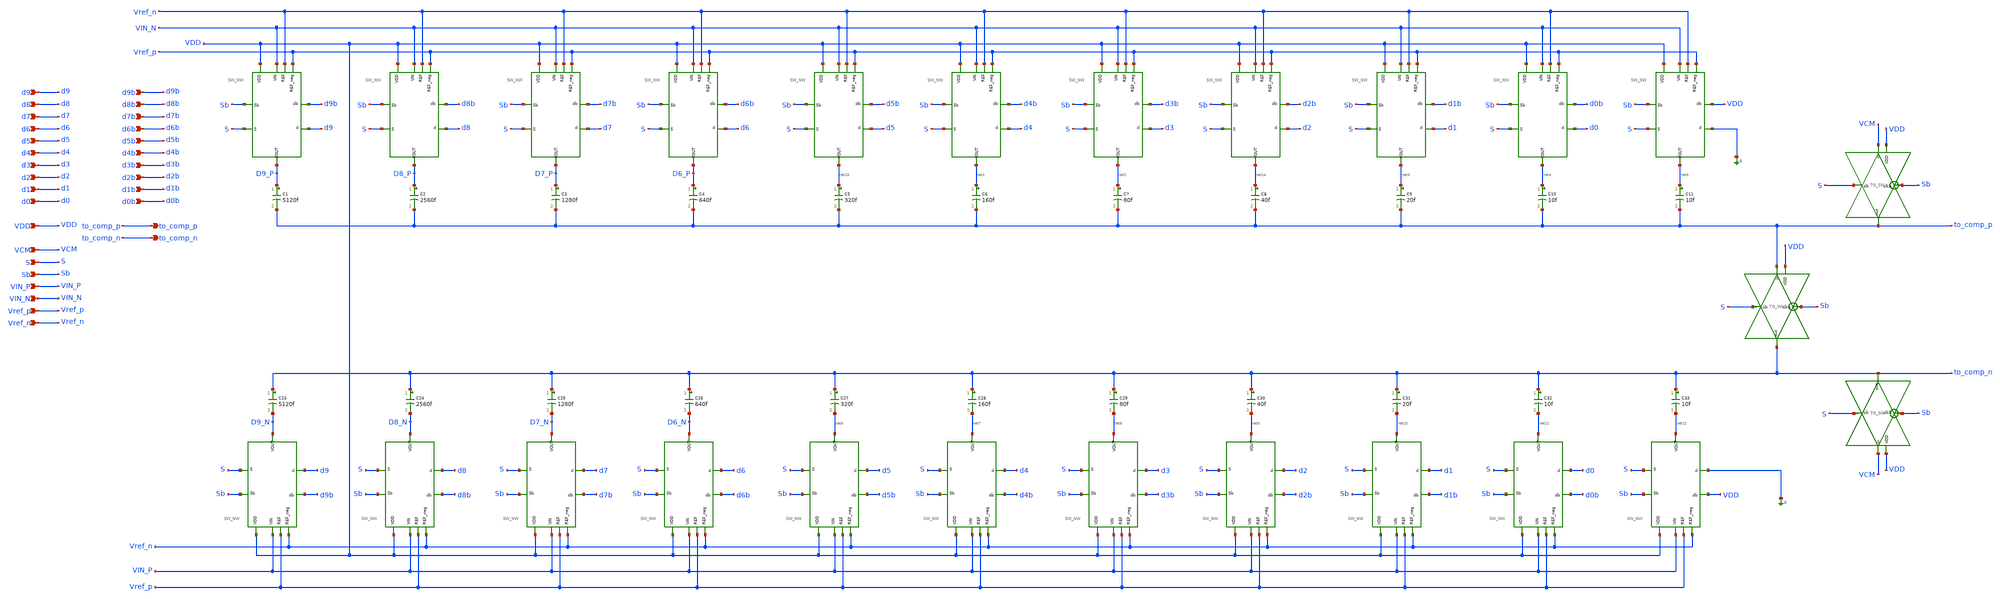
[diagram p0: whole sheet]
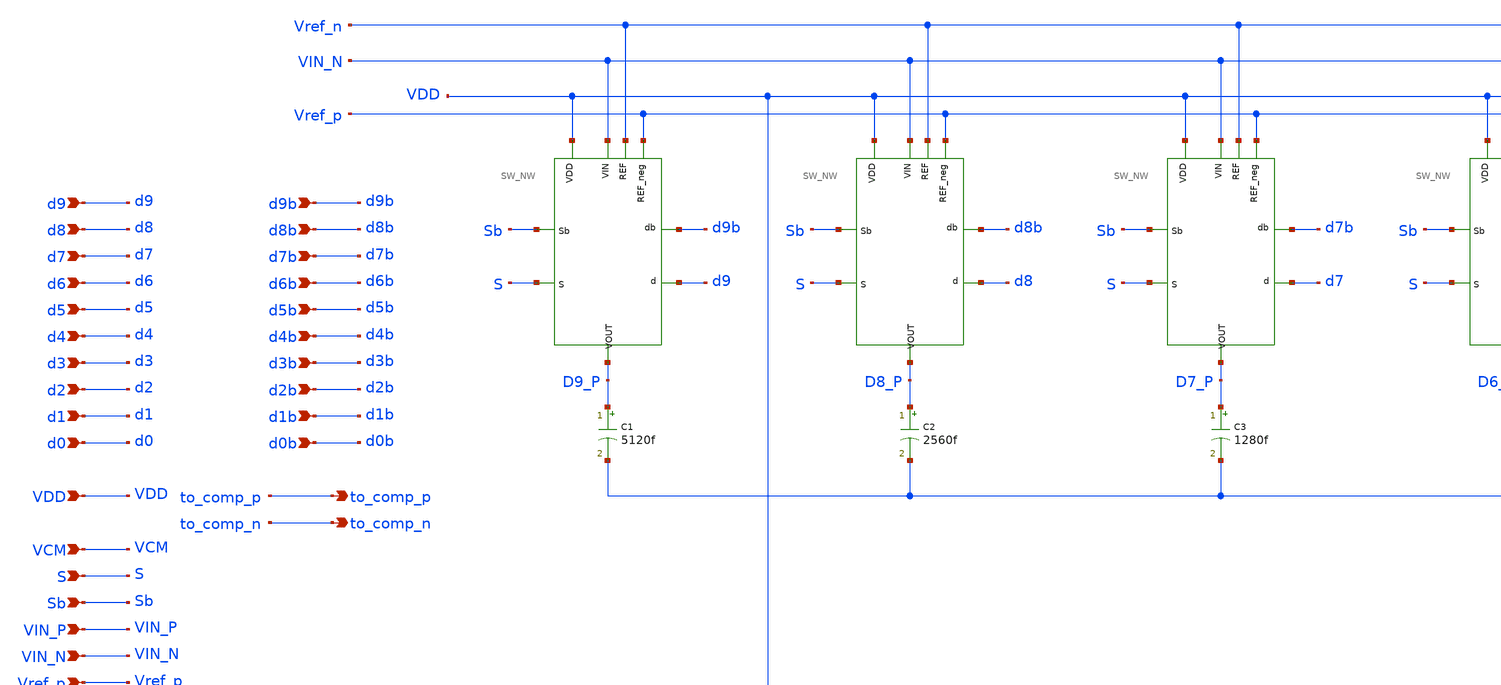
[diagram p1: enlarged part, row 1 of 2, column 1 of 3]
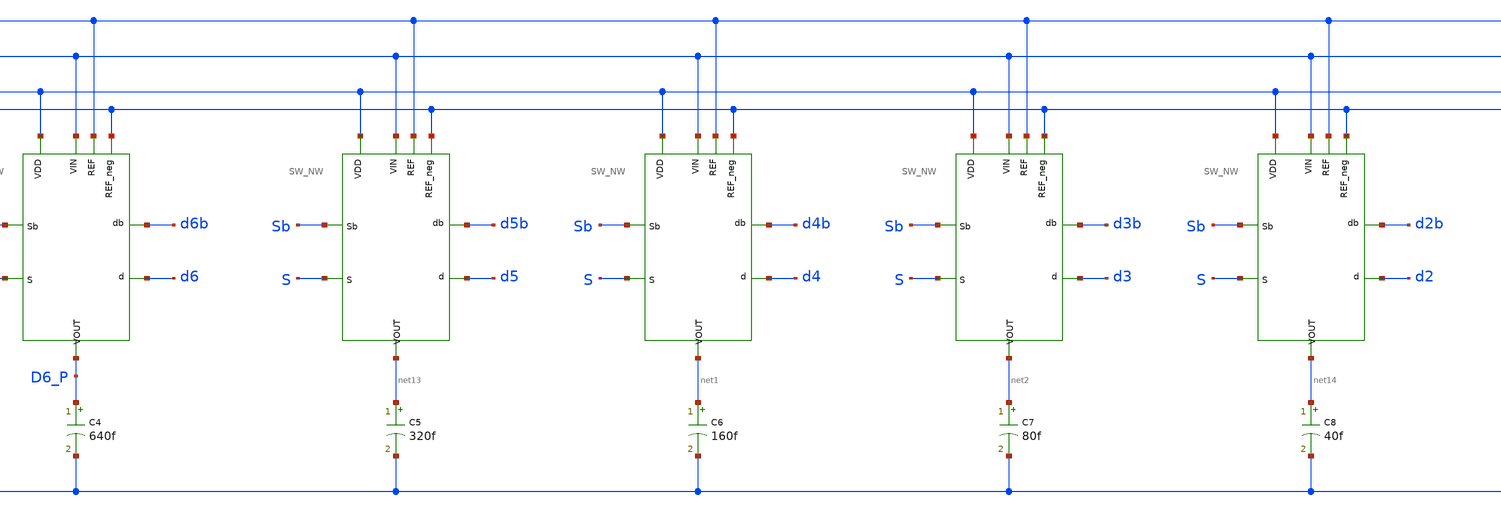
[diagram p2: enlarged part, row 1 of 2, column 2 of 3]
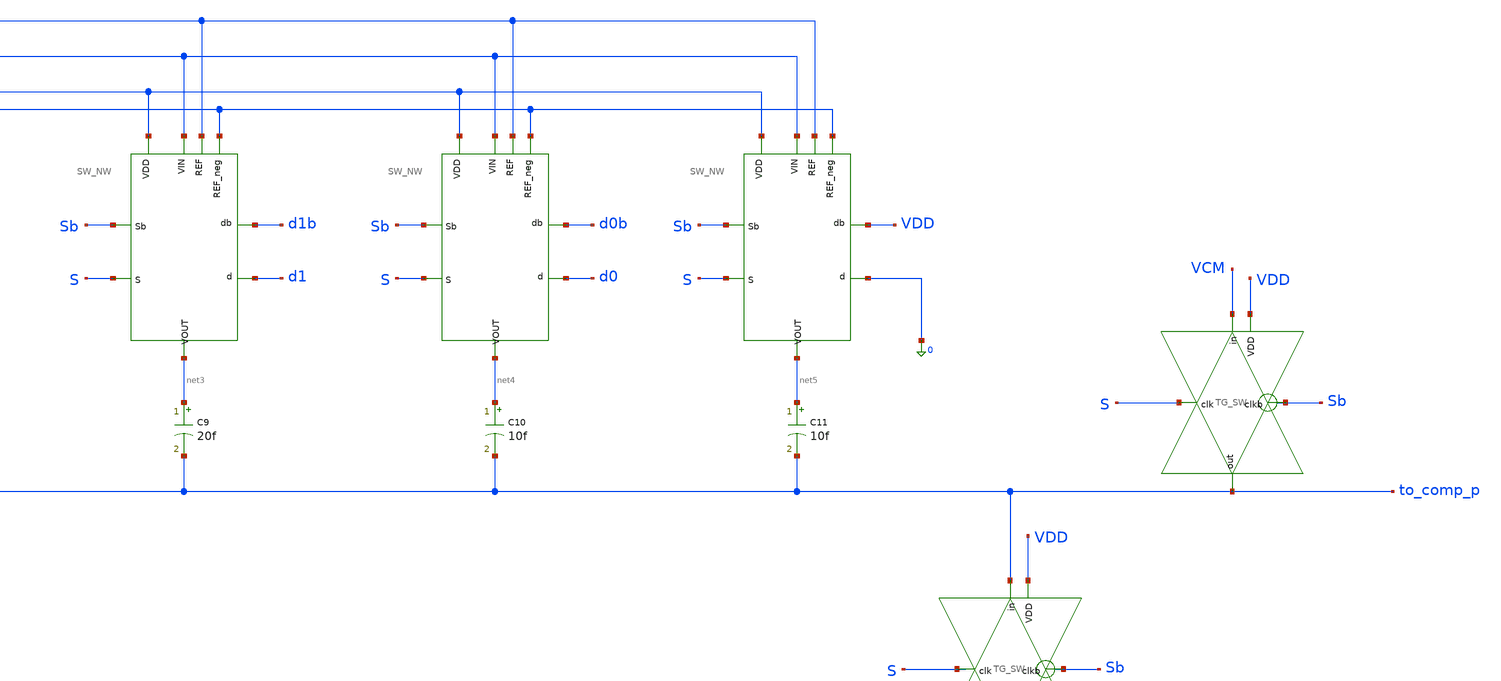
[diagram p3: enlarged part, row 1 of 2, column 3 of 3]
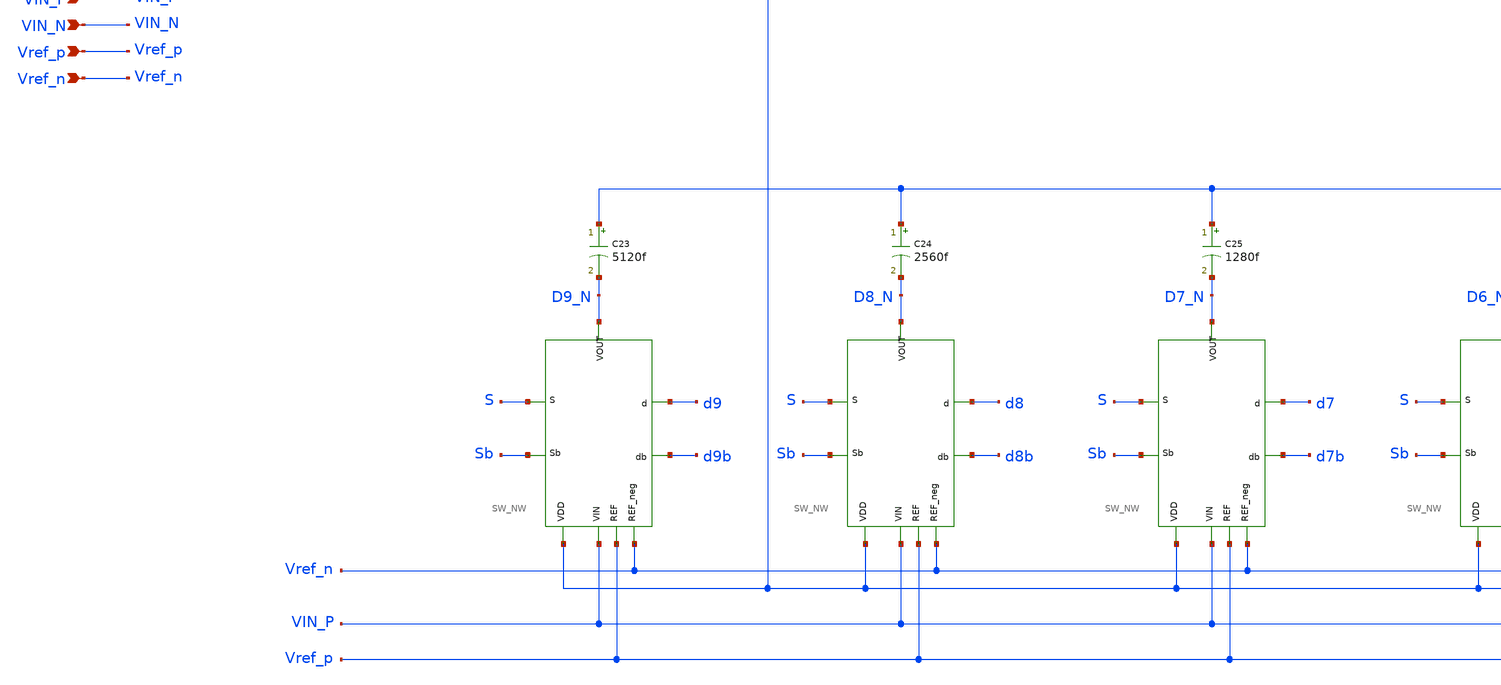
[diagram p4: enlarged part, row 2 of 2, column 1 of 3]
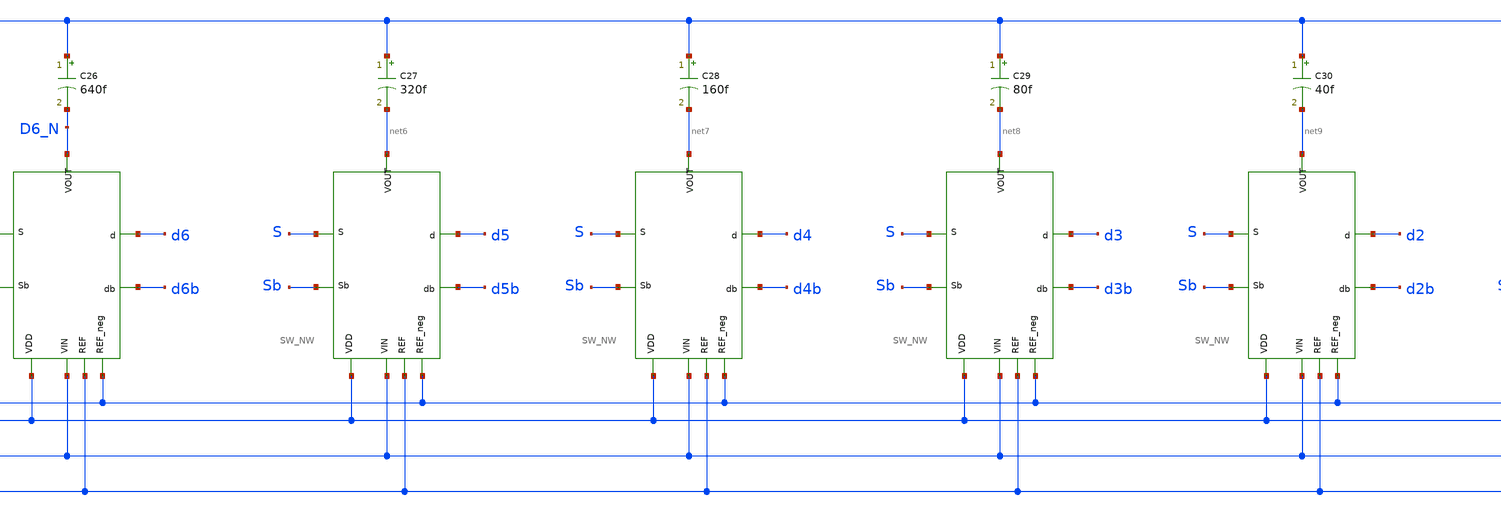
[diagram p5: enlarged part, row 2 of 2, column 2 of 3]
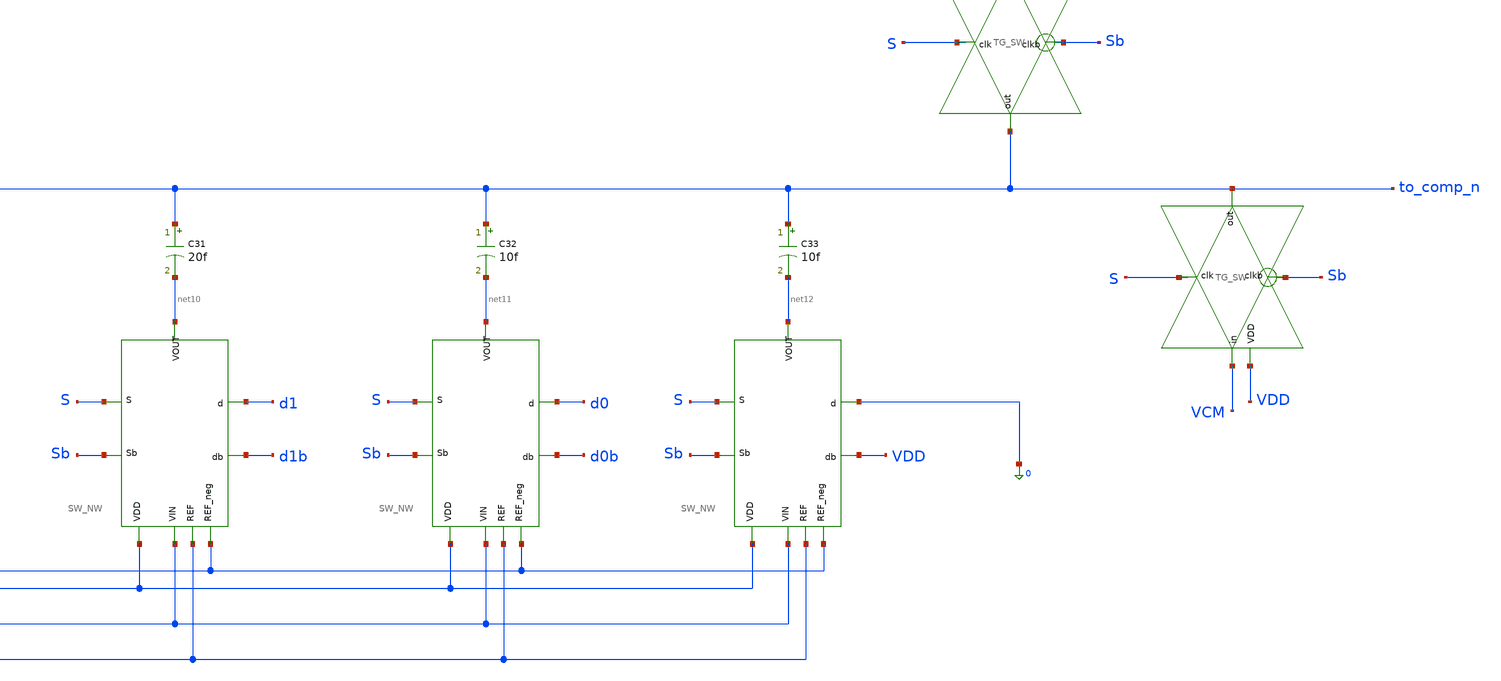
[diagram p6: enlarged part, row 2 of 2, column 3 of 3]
** sch_path: Design_Files/IC Design/Schematic/SAR_ADC_BLOCKS/CDAC/CDAC.sch
**.subckt CDAC d7 d7b d6 d6b d9 d9b d8 d8b d3 d3b d2 d2b d5 d5b d4 d4b d1 d1b d0 d0b VCM S VDD VIN_N
*+ Vref_p Sb VIN_P Vref_n to_comp_p to_comp_n
*.ipin d7
*.ipin d7b
*.ipin d6
*.ipin d6b
*.ipin d9
*.ipin d9b
*.ipin d8
*.ipin d8b
*.ipin d3
*.ipin d3b
*.ipin d2
*.ipin d2b
*.ipin d5
*.ipin d5b
*.ipin d4
*.ipin d4b
*.ipin d1
*.ipin d1b
*.ipin d0
*.ipin d0b
*.ipin VCM
*.ipin S
*.ipin VDD
*.ipin VIN_N
*.ipin Vref_p
*.ipin Sb
*.ipin VIN_P
*.ipin Vref_n
*.opin to_comp_p
*.opin to_comp_n
C1 D9_P to_comp_p 5120f m=1
C2 D8_P to_comp_p 2560f m=1
C3 D7_P to_comp_p 1280f m=1
C4 D6_P to_comp_p 640f m=1
C5 net13 to_comp_p 320f m=1
C6 net1 to_comp_p 160f m=1
C7 net2 to_comp_p 80f m=1
C8 net14 to_comp_p 40f m=1
C9 net3 to_comp_p 20f m=1
C10 net4 to_comp_p 10f m=1
C11 net5 to_comp_p 10f m=1
C23 to_comp_n D9_N 5120f m=1
C24 to_comp_n D8_N 2560f m=1
C25 to_comp_n D7_N 1280f m=1
C26 to_comp_n D6_N 640f m=1
C27 to_comp_n net6 320f m=1
C28 to_comp_n net7 160f m=1
C29 to_comp_n net8 80f m=1
C30 to_comp_n net9 40f m=1
C31 to_comp_n net10 20f m=1
C32 to_comp_n net11 10f m=1
C33 to_comp_n net12 10f m=1
xSWNW1 d9 d9b S Sb Vref_p Vref_n VIN_N D9_P VDD SW_NW
xSWNW2 d8 d8b S Sb Vref_p Vref_n VIN_N D8_P VDD SW_NW
xSWNW3 d7 d7b S Sb Vref_p Vref_n VIN_N D7_P VDD SW_NW
xSWNW4 d6 d6b S Sb Vref_p Vref_n VIN_N D6_P VDD SW_NW
xSWNW5 d5 d5b S Sb Vref_p Vref_n VIN_N net13 VDD SW_NW
xSWNW6 d4 d4b S Sb Vref_p Vref_n VIN_N net1 VDD SW_NW
xSWNW7 d3 d3b S Sb Vref_p Vref_n VIN_N net2 VDD SW_NW
xSWNW8 d2 d2b S Sb Vref_p Vref_n VIN_N net14 VDD SW_NW
xSWNW9 d1 d1b S Sb Vref_p Vref_n VIN_N net3 VDD SW_NW
xSWNW10 d0 d0b S Sb Vref_p Vref_n VIN_N net4 VDD SW_NW
xSWNW11 0 VDD S Sb Vref_p Vref_n VIN_N net5 VDD SW_NW
xSWNW12 d9 d9b S Sb Vref_n Vref_p VIN_P D9_N VDD SW_NW
xSWNW13 d8 d8b S Sb Vref_n Vref_p VIN_P D8_N VDD SW_NW
xSWNW14 d7 d7b S Sb Vref_n Vref_p VIN_P D7_N VDD SW_NW
xSWNW15 d6 d6b S Sb Vref_n Vref_p VIN_P D6_N VDD SW_NW
xSWNW16 d5 d5b S Sb Vref_n Vref_p VIN_P net6 VDD SW_NW
xSWNW17 d4 d4b S Sb Vref_n Vref_p VIN_P net7 VDD SW_NW
xSWNW18 d3 d3b S Sb Vref_n Vref_p VIN_P net8 VDD SW_NW
xSWNW19 d2 d2b S Sb Vref_n Vref_p VIN_P net9 VDD SW_NW
xSWNW20 d1 d1b S Sb Vref_n Vref_p VIN_P net10 VDD SW_NW
xSWNW21 d0 d0b S Sb Vref_n Vref_p VIN_P net11 VDD SW_NW
xSWNW22 0 VDD S Sb Vref_n Vref_p VIN_P net12 VDD SW_NW
xTGSW1 S to_comp_p to_comp_n VDD Sb TG_SW
xTGSW2 S VCM to_comp_n VDD Sb TG_SW
xTGSW3 S VCM to_comp_p VDD Sb TG_SW
**.ends

* expanding   symbol:  ECG_Acquisition_IC/Design_Files/IC
*+ Design/Schematic/SAR_ADC_BLOCKS/SW_NW/SW_NW.sym # of pins=9
** sym_path: Design_Files/IC Design/Schematic/SAR_ADC_BLOCKS/SW_NW/SW_NW.sym
** sch_path: Design_Files/IC Design/Schematic/SAR_ADC_BLOCKS/SW_NW/SW_NW.sch
.subckt SW_NW d db S Sb REF_neg REF VIN VOUT VDD
*.ipin S
*.ipin db
*.ipin d
*.ipin Sb
*.ipin VIN
*.ipin REF
*.ipin REF_neg
*.ipin VOUT
*.ipin VDD
xTGSW1 S VIN VOUT VDD Sb TG_SW
xTGSW2 Sb net1 VOUT VDD S TG_SW
xTGSW3 d REF net1 VDD db TG_SW
xTGSW4 db REF_neg net1 VDD d TG_SW
.ends


* expanding   symbol:  ECG_Acquisition_IC/Design_Files/IC
*+ Design/Schematic/SAR_ADC_BLOCKS/TG_SW/TG_SW.sym # of pins=5
** sym_path: Design_Files/IC Design/Schematic/SAR_ADC_BLOCKS/TG_SW/TG_SW.sym
** sch_path: Design_Files/IC Design/Schematic/SAR_ADC_BLOCKS/TG_SW/TG_SW.sch
.subckt TG_SW clk in out VDD clkb
*.ipin in
*.ipin clk
*.ipin clkb
*.opin out
*.ipin VDD
XM1 out clk in 0 nfet_03v3 L=0.28u W=0.28u nf=1 ad='int((nf+1)/2) * W/nf * 0.18u' as='int((nf+2)/2) * W/nf * 0.18u'
+ pd='2*int((nf+1)/2) * (W/nf + 0.18u)' ps='2*int((nf+2)/2) * (W/nf + 0.18u)' nrd='0.18u / W' nrs='0.18u / W'
+ sa=0 sb=0 sd=0 m=1
XM2 out clkb in VDD pfet_03v3 L=0.28u W=0.28u nf=1 ad='int((nf+1)/2) * W/nf * 0.18u' as='int((nf+2)/2) * W/nf * 0.18u'
+ pd='2*int((nf+1)/2) * (W/nf + 0.18u)' ps='2*int((nf+2)/2) * (W/nf + 0.18u)' nrd='0.18u / W' nrs='0.18u / W'
+ sa=0 sb=0 sd=0 m=1
.ends

.end
